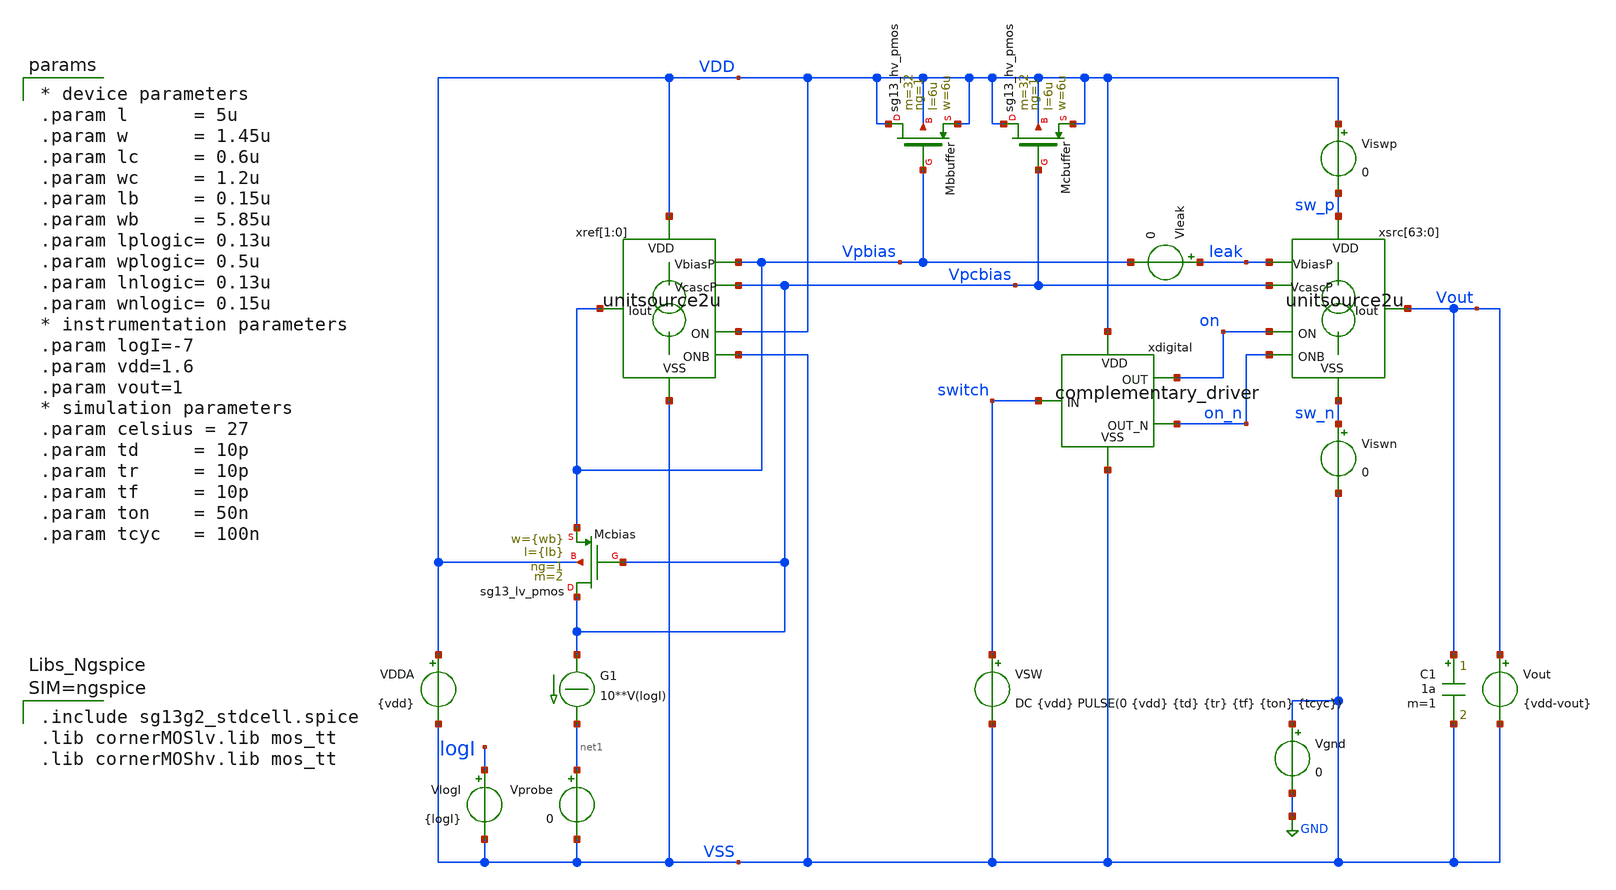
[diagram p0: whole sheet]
** sch_path: xschem/test_unitsource2u_DC.sch
**.subckt test_unitsource2u_DC
Vout Vout VSS {vdd-vout}
.save i(vout)
Vprobe net1 VSS 0
.save i(vprobe)
G1 Vpcbias net1 CUR=' 10**V(logI) '
VlogI logI VSS {logI}
.save i(vlogi)
VDDA VDD VSS {vdd}
.save i(vdda)
XMcbias Vpcbias Vpcbias Vpbias VDD sg13_lv_pmos w={wb} l={lb} ng=1 m=2 mm_ok=1
VSW switch VSS DC {vdd} PULSE(0 {vdd} {td} {tr} {tf} {ton} {tcyc})
.save i(vsw)
XMcbuffer VDD Vpcbias VDD VDD sg13_hv_pmos w=6u l=6u ng=1 m=32 mm_ok=1
XMbbuffer VDD Vpbias VDD VDD sg13_hv_pmos w=6u l=6u ng=1 m=32 mm_ok=1
xref[1] VDD Vpbias VDD VSS Vpbias Vpcbias VSS unitsource2u
xref[0] VDD Vpbias VDD VSS Vpbias Vpcbias VSS unitsource2u
xsrc[63] sw_p leak on on_n Vout Vpcbias sw_n unitsource2u
xsrc[62] sw_p leak on on_n Vout Vpcbias sw_n unitsource2u
xsrc[61] sw_p leak on on_n Vout Vpcbias sw_n unitsource2u
xsrc[60] sw_p leak on on_n Vout Vpcbias sw_n unitsource2u
xsrc[59] sw_p leak on on_n Vout Vpcbias sw_n unitsource2u
xsrc[58] sw_p leak on on_n Vout Vpcbias sw_n unitsource2u
xsrc[57] sw_p leak on on_n Vout Vpcbias sw_n unitsource2u
xsrc[56] sw_p leak on on_n Vout Vpcbias sw_n unitsource2u
xsrc[55] sw_p leak on on_n Vout Vpcbias sw_n unitsource2u
xsrc[54] sw_p leak on on_n Vout Vpcbias sw_n unitsource2u
xsrc[53] sw_p leak on on_n Vout Vpcbias sw_n unitsource2u
xsrc[52] sw_p leak on on_n Vout Vpcbias sw_n unitsource2u
xsrc[51] sw_p leak on on_n Vout Vpcbias sw_n unitsource2u
xsrc[50] sw_p leak on on_n Vout Vpcbias sw_n unitsource2u
xsrc[49] sw_p leak on on_n Vout Vpcbias sw_n unitsource2u
xsrc[48] sw_p leak on on_n Vout Vpcbias sw_n unitsource2u
xsrc[47] sw_p leak on on_n Vout Vpcbias sw_n unitsource2u
xsrc[46] sw_p leak on on_n Vout Vpcbias sw_n unitsource2u
xsrc[45] sw_p leak on on_n Vout Vpcbias sw_n unitsource2u
xsrc[44] sw_p leak on on_n Vout Vpcbias sw_n unitsource2u
xsrc[43] sw_p leak on on_n Vout Vpcbias sw_n unitsource2u
xsrc[42] sw_p leak on on_n Vout Vpcbias sw_n unitsource2u
xsrc[41] sw_p leak on on_n Vout Vpcbias sw_n unitsource2u
xsrc[40] sw_p leak on on_n Vout Vpcbias sw_n unitsource2u
xsrc[39] sw_p leak on on_n Vout Vpcbias sw_n unitsource2u
xsrc[38] sw_p leak on on_n Vout Vpcbias sw_n unitsource2u
xsrc[37] sw_p leak on on_n Vout Vpcbias sw_n unitsource2u
xsrc[36] sw_p leak on on_n Vout Vpcbias sw_n unitsource2u
xsrc[35] sw_p leak on on_n Vout Vpcbias sw_n unitsource2u
xsrc[34] sw_p leak on on_n Vout Vpcbias sw_n unitsource2u
xsrc[33] sw_p leak on on_n Vout Vpcbias sw_n unitsource2u
xsrc[32] sw_p leak on on_n Vout Vpcbias sw_n unitsource2u
xsrc[31] sw_p leak on on_n Vout Vpcbias sw_n unitsource2u
xsrc[30] sw_p leak on on_n Vout Vpcbias sw_n unitsource2u
xsrc[29] sw_p leak on on_n Vout Vpcbias sw_n unitsource2u
xsrc[28] sw_p leak on on_n Vout Vpcbias sw_n unitsource2u
xsrc[27] sw_p leak on on_n Vout Vpcbias sw_n unitsource2u
xsrc[26] sw_p leak on on_n Vout Vpcbias sw_n unitsource2u
xsrc[25] sw_p leak on on_n Vout Vpcbias sw_n unitsource2u
xsrc[24] sw_p leak on on_n Vout Vpcbias sw_n unitsource2u
xsrc[23] sw_p leak on on_n Vout Vpcbias sw_n unitsource2u
xsrc[22] sw_p leak on on_n Vout Vpcbias sw_n unitsource2u
xsrc[21] sw_p leak on on_n Vout Vpcbias sw_n unitsource2u
xsrc[20] sw_p leak on on_n Vout Vpcbias sw_n unitsource2u
xsrc[19] sw_p leak on on_n Vout Vpcbias sw_n unitsource2u
xsrc[18] sw_p leak on on_n Vout Vpcbias sw_n unitsource2u
xsrc[17] sw_p leak on on_n Vout Vpcbias sw_n unitsource2u
xsrc[16] sw_p leak on on_n Vout Vpcbias sw_n unitsource2u
xsrc[15] sw_p leak on on_n Vout Vpcbias sw_n unitsource2u
xsrc[14] sw_p leak on on_n Vout Vpcbias sw_n unitsource2u
xsrc[13] sw_p leak on on_n Vout Vpcbias sw_n unitsource2u
xsrc[12] sw_p leak on on_n Vout Vpcbias sw_n unitsource2u
xsrc[11] sw_p leak on on_n Vout Vpcbias sw_n unitsource2u
xsrc[10] sw_p leak on on_n Vout Vpcbias sw_n unitsource2u
xsrc[9] sw_p leak on on_n Vout Vpcbias sw_n unitsource2u
xsrc[8] sw_p leak on on_n Vout Vpcbias sw_n unitsource2u
xsrc[7] sw_p leak on on_n Vout Vpcbias sw_n unitsource2u
xsrc[6] sw_p leak on on_n Vout Vpcbias sw_n unitsource2u
xsrc[5] sw_p leak on on_n Vout Vpcbias sw_n unitsource2u
xsrc[4] sw_p leak on on_n Vout Vpcbias sw_n unitsource2u
xsrc[3] sw_p leak on on_n Vout Vpcbias sw_n unitsource2u
xsrc[2] sw_p leak on on_n Vout Vpcbias sw_n unitsource2u
xsrc[1] sw_p leak on on_n Vout Vpcbias sw_n unitsource2u
xsrc[0] sw_p leak on on_n Vout Vpcbias sw_n unitsource2u
Viswp VDD sw_p 0
.save i(viswp)
Viswn sw_n VSS 0
.save i(viswn)
C1 Vout VSS 1a m=1
Vgnd VSS GND 0
.save i(vgnd)
Vleak leak Vpbias 0
.save i(vleak)
xdigital VDD on switch on_n VSS complementary_driver
**** begin user architecture code


.include test_unitsource2u_DC.save
.temp={celsius}
.options gmin=1e-15 abstol=1p method=gear
.options savecurrents
.control
save all
op
write test_unitsource2u_DC.raw
set appendwrite
dc Vout 0 1.6 10m VlogI -8 -5 0.5
*tran 10p 500n
write test_unitsource2u_DC.raw
plot title "voltages" vdd vpbias vpcbias switch on_n on vout
plot title "switch voltages" switch on on_n xsrc.on_n xsrc.off_n xsrc.vcasc xref.drain
+ xsrc.xsrc.drain
*plot @n.xsw.xmbias.nsg13_lv_pmos[ids] @n.xsw.xmpullup.nsg13_lv_pmos[ids]
plot title "digital switch block currents" viswp#branch-vout#branch viswn#branch
plot title "switch cross and difference currents" 0.5*(viswp#branch+viswn#branch-vout#branch)
+ viswp#branch-viswn#branch-vout#branch
plot title "Vpbias leakage" vleak#branch
plot title "output and reference currents" vout#branch vprobe#branch
plot title "output current accuracy" 2*(vout#branch/32-vprobe#branch)/(vprobe#branch+vout#branch/32)
plot title "output current accuracy" ylimit -40m 40m
+ 2*(vout#branch/32-vprobe#branch)/(vprobe#branch+vout#branch/32)
.endc




.include sg13g2_stdcell.spice
.lib cornerMOSlv.lib mos_tt
.lib cornerMOShv.lib mos_tt



* device parameters
.param l      = 5u
.param w      = 1.45u
.param lc     = 0.6u
.param wc     = 1.2u
.param lb     = 0.15u
.param wb     = 5.85u
.param lplogic= 0.13u
.param wplogic= 0.5u
.param lnlogic= 0.13u
.param wnlogic= 0.15u
* instrumentation parameters
.param logI=-7
.param vdd=1.6
.param vout=1
* simulation parameters
.param celsius = 27
.param td     = 10p
.param tr     = 10p
.param tf     = 10p
.param ton    = 50n
.param tcyc   = 100n


**** end user architecture code
**.ends

* expanding   symbol:  unitsource2u.sym # of pins=7
** sym_path: xschem/unitsource2u.sym
** sch_path: xschem/unitsource2u.sch
.subckt unitsource2u VDD VbiasP ON ONB Iout VcascP VSS
*.iopin VSS
*.iopin VDD
*.iopin VbiasP
*.iopin VcascP
*.ipin ON
*.ipin ONB
*.iopin Iout
xnonoverlap VDD VSS ON ONB on_n off_n nonoverlap
xsw VDD off_n Vcasc on_n VcascP cascodeswitch_pmos
xsrc VDD VbiasP Vcasc Iout pcsource2u
.ends


* expanding   symbol:  complementary_driver.sym # of pins=5
** sym_path: xschem/complementary_driver.sym
** sch_path: xschem/complementary_driver.sch
.subckt complementary_driver VDD OUT IN OUT_N VSS
*.iopin VSS
*.iopin VDD
*.ipin IN
*.opin OUT
*.opin OUT_N
x0 OUT_N IN VDD VSS sg13g2_inv_1
x1 OUT OUT_N VDD VSS sg13g2_inv_1
.ends


* expanding   symbol:  nonoverlap.sym # of pins=6
** sym_path: xschem/nonoverlap.sym
** sch_path: xschem/nonoverlap.sch
.subckt nonoverlap VDD VSS INP INN OUTN OUTP
*.iopin VSS
*.iopin VDD
*.ipin INP
*.ipin INN
*.opin OUTP
*.opin OUTN
XM1 OUTN INP VDD VDD sg13_lv_pmos w=0.3u l=0.13u ng=1 m=1 mm_ok=1
XM2 OUTP INN VDD VDD sg13_lv_pmos w=0.3u l=0.13u ng=1 m=1 mm_ok=1
XM3 OUTN OUTP VSS VSS sg13_lv_nmos w=0.15u l=0.52u ng=1 m=1 mm_ok=1
XM4 OUTP OUTN VSS VSS sg13_lv_nmos w=0.15u l=0.52u ng=1 m=1 mm_ok=1
.ends


* expanding   symbol:  cascodeswitch_pmos.sym # of pins=5
** sym_path: xschem/cascodeswitch_pmos.sym
** sch_path: xschem/cascodeswitch_pmos.sch
.subckt cascodeswitch_pmos VDD off_n Vcasc on_n Vbpcasc
*.ipin off_n
*.ipin Vbpcasc
*.opin Vcasc
*.ipin on_n
*.ipin VDD
XMpullup Vcasc off_n VDD VDD sg13_lv_pmos w=0.3u l=0.13u ng=1 m=1 mm_ok=1
XMbias Vbpcasc on_n Vcasc VDD sg13_lv_pmos w=0.3u l=0.13u ng=1 m=1 mm_ok=1
.ends


* expanding   symbol:  pcsource2u.sym # of pins=4
** sym_path: xschem/pcsource2u.sym
** sch_path: xschem/pcsource2u.sch
.subckt pcsource2u VDD VbiasP VcascodeP Iout
*.ipin VcascodeP
*.ipin VbiasP
*.opin Iout
*.ipin VDD
XMsrc drain net4 VDD net1 sg13_lv_pmos w=1.45u l=5u ng=1 m=1 mm_ok=1
XMcasc Iout net3 drain net2 sg13_lv_pmos w=1.2u l=0.6u ng=1 m=1 mm_ok=1
Vgsrc net4 VbiasP 0
.save i(vgsrc)
Vgcasc net3 VcascodeP 0
.save i(vgcasc)
Vbsrc VDD net1 0
.save i(vbsrc)
Vbcasc VDD net2 0
.save i(vbcasc)
.ends


* expanding   symbol:  sg13g2_stdcells/sg13g2_inv_1.sym # of pins=2
** sym_path: sg13g2_stdcells/sg13g2_inv_1.sym
** sch_path: sg13g2_stdcells/sg13g2_inv_1.sch
.subckt sg13g2_inv_1 Y A VDD VSS
*.opin Y
*.ipin A
*.iopin VDD
*.iopin VSS
XM1 Y A VSS VSS sg13_lv_nmos w=740.00n l=130.00n ng=1 m=1 mm_ok=1
XM2 Y A VDD VDD sg13_lv_pmos w=1.12u l=130.00n ng=1 m=1 mm_ok=1
.ends

.GLOBAL GND
.end
